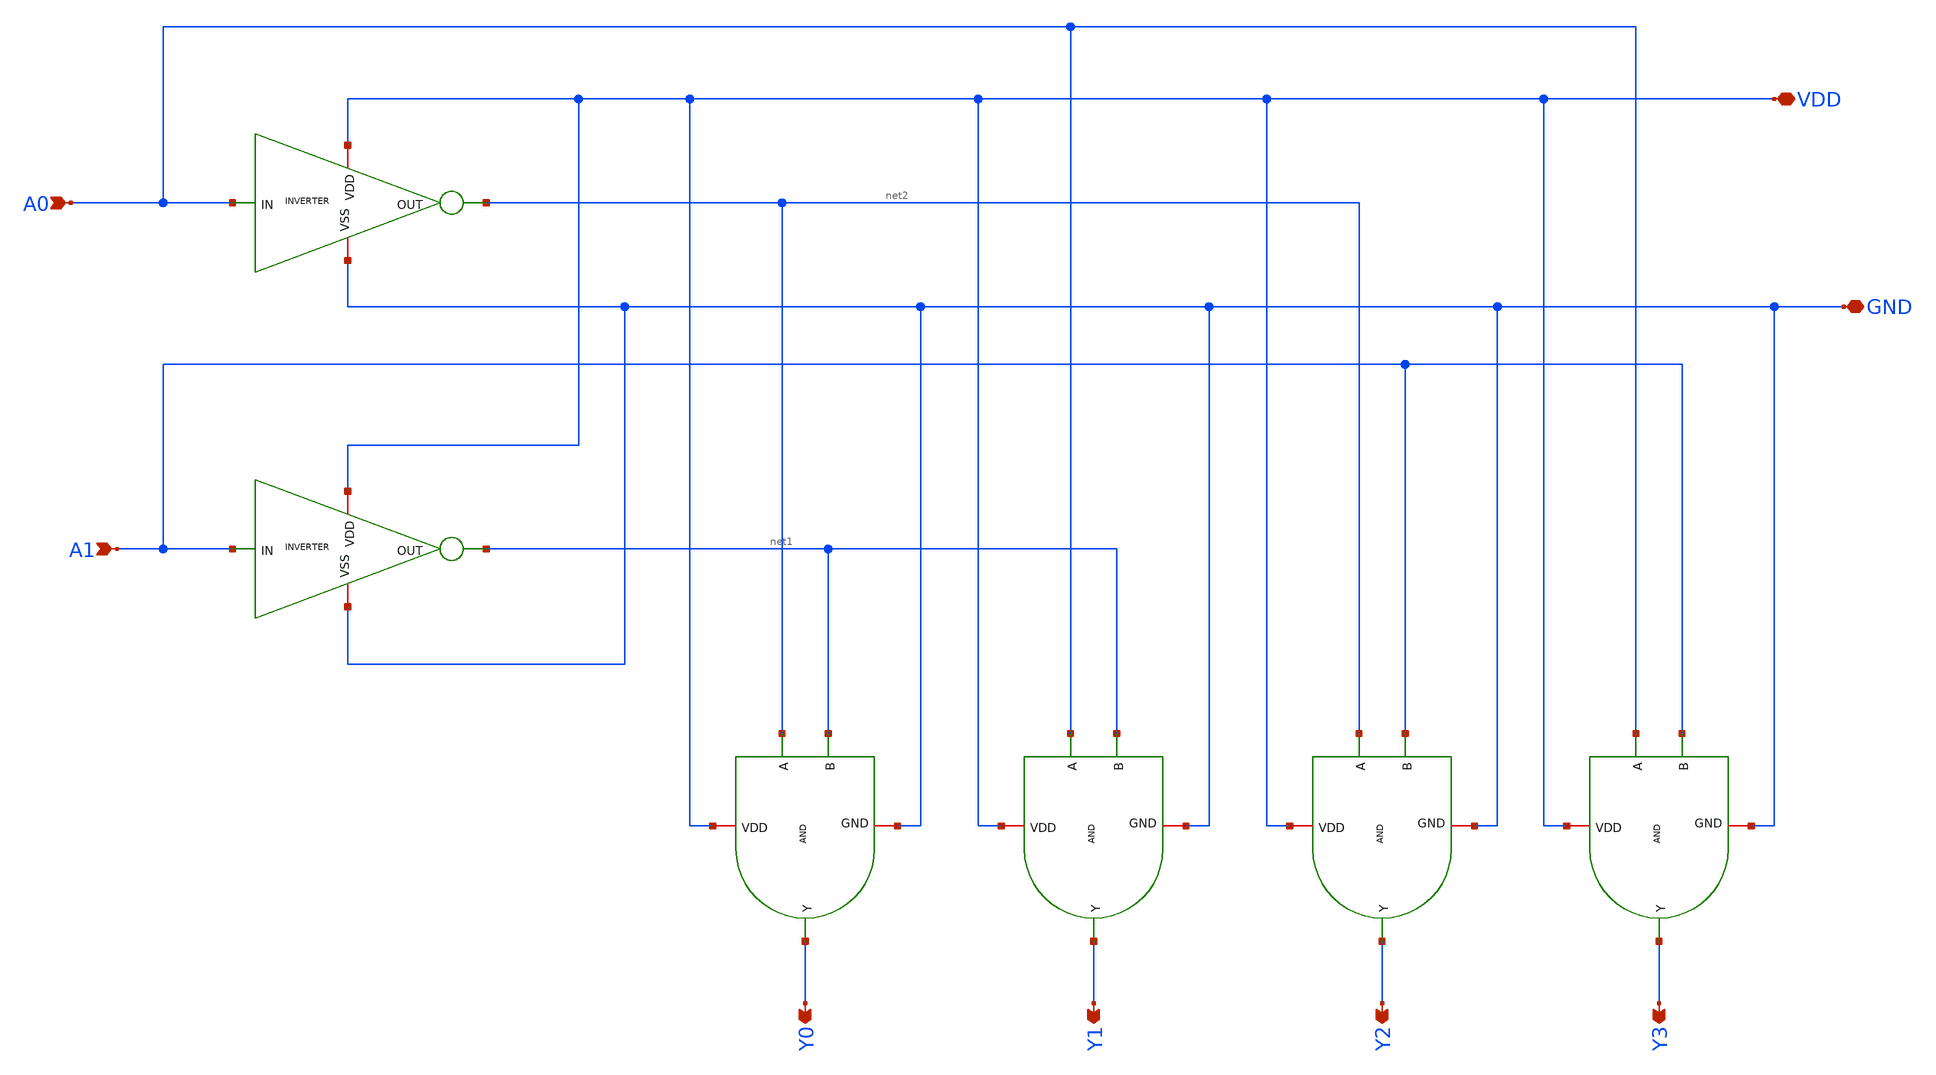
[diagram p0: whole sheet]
** sch_path: DECODER3TO8/Schematic/DECODER2_TO_4.sch
**.subckt DECODER2_TO_4 A0 A1 Y0 Y1 Y2 Y3 VDD GND
*.ipin A0
*.ipin A1
*.opin Y0
*.opin Y1
*.opin Y2
*.opin Y3
*.iopin VDD
*.iopin GND
x1 VDD A0 net2 GND INVERTER
x2 VDD A1 net1 GND INVERTER
x3 VDD net2 Y0 net1 GND AND
x4 VDD A0 Y1 net1 GND AND
x5 VDD net2 Y2 A1 GND AND
x6 VDD A0 Y3 A1 GND AND
**.ends
.end
